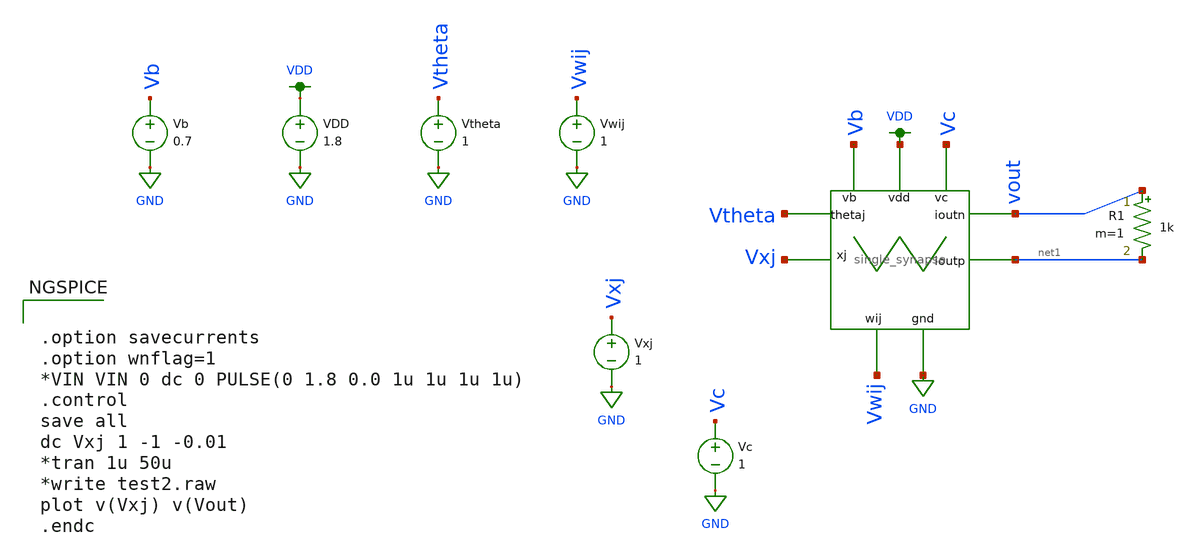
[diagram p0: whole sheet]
** sch_path: test_single_synapse.sch
**.subckt test_single_synapse
VDD VDD GND 1.8
Vb Vb GND 0.7
Vc Vc GND 1
W1 Vtheta Vb VDD Vc Vxj GND Vwij vout net1 single_synapse
Vtheta Vtheta GND 1
Vwij Vwij GND 1
Vxj Vxj GND 1
R1 vout net1 1k m=1
**** begin user architecture code


.option savecurrents
.option wnflag=1
*VIN VIN 0 dc 0 PULSE(0 1.8 0.0 1u 1u 1u 1u)
.control
save all
dc Vxj 1 -1 -0.01
*tran 1u 50u
*write test2.raw
plot v(Vxj) v(Vout)
.endc



** opencircuitdesign pdks install
.lib $::SKYWATER_MODELS/sky130.lib.spice tt


**** end user architecture code
**.ends
.GLOBAL VDD
.GLOBAL GND
.end
